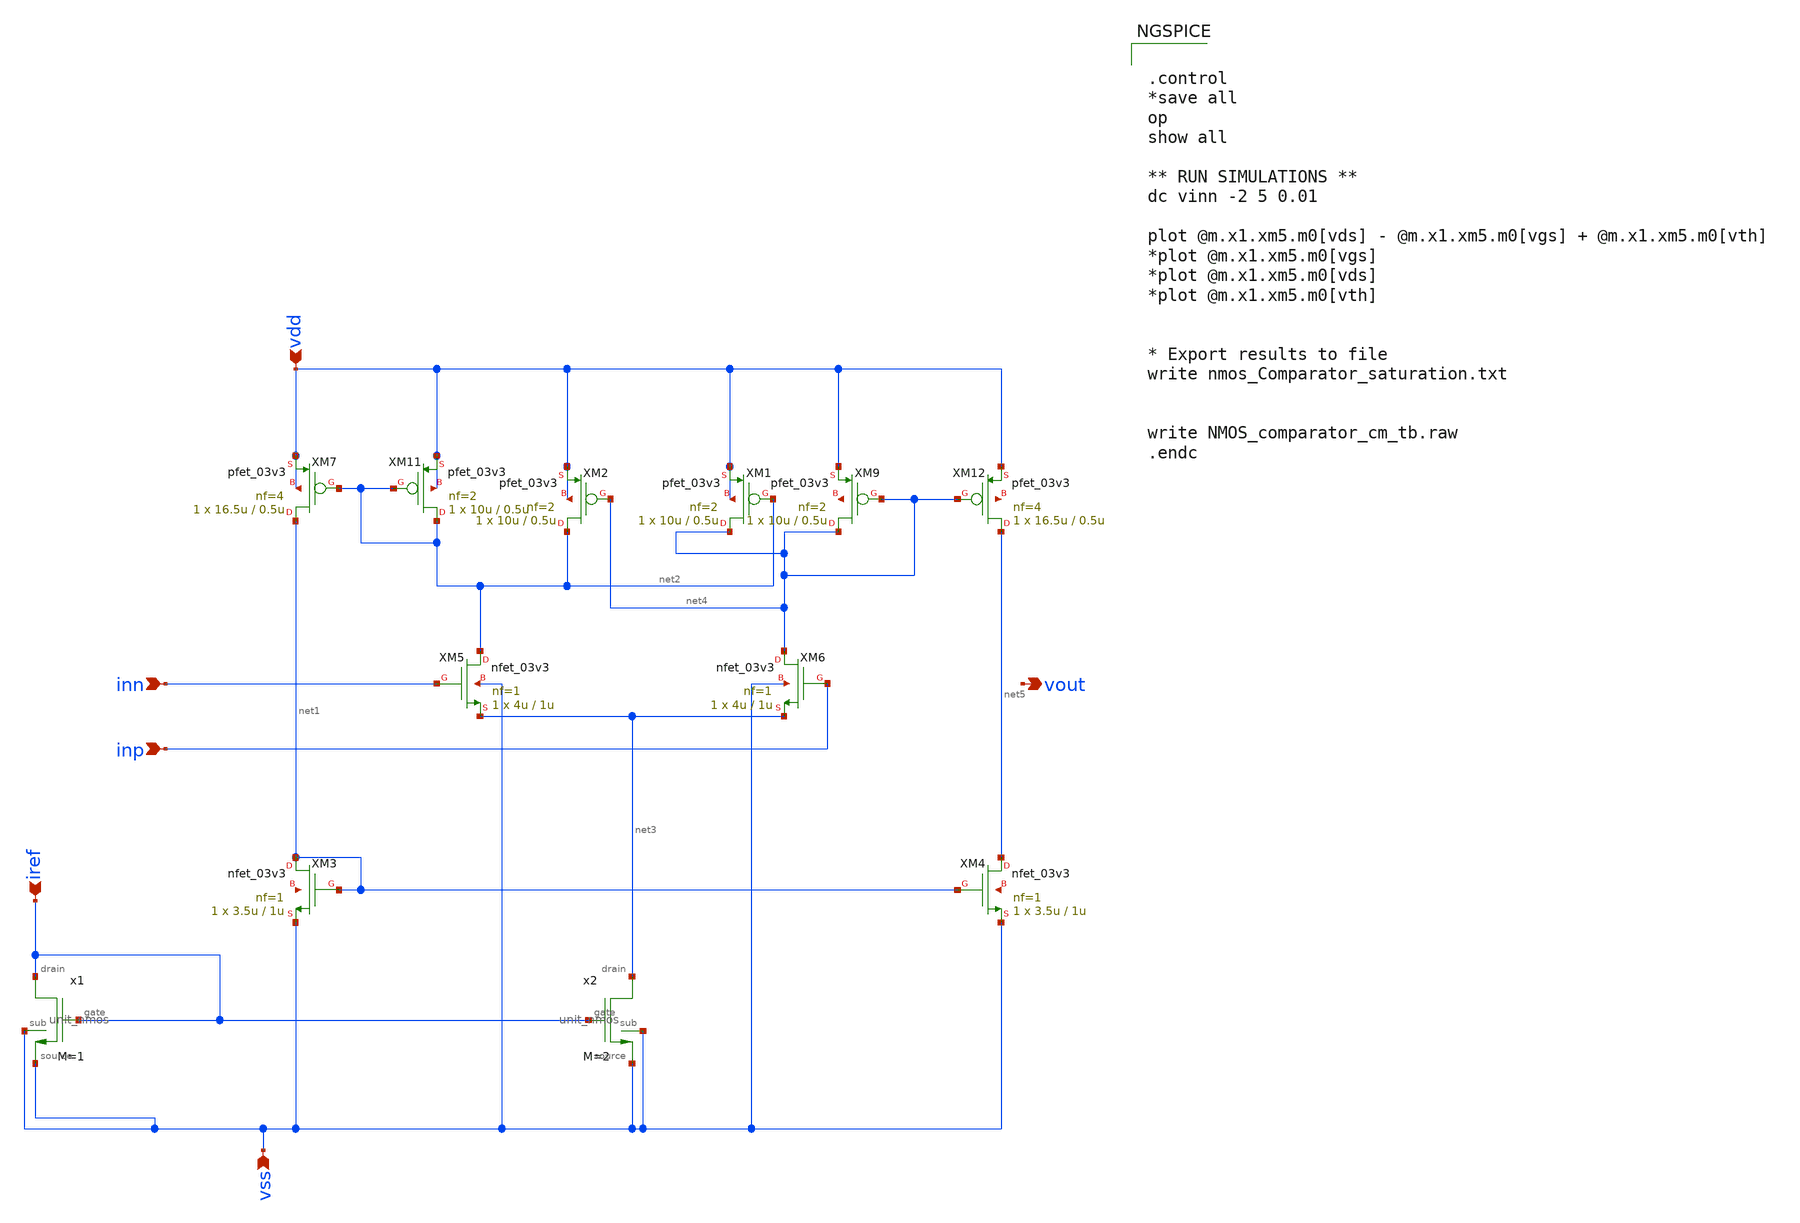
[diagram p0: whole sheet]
** sch_path: designs/libs/core_analog/Comparator/Nmos_Comparator.sch
**.subckt Nmos_Comparator vss vdd iref inn inp vout
*.ipin vss
*.ipin vdd
*.ipin iref
*.ipin inn
*.ipin inp
*.opin vout
XM3 net1 net1 vss net6 nfet_03v3 L=1u W=3.5u nf=1 ad='int((nf+1)/2) * W/nf * 0.18u' as='int((nf+2)/2) * W/nf * 0.18u'
+ pd='2*int((nf+1)/2) * (W/nf + 0.18u)' ps='2*int((nf+2)/2) * (W/nf + 0.18u)' nrd='0.18u / W' nrs='0.18u / W'
+ sa=0 sb=0 sd=0 m=1
XM4 net5 net1 vss net7 nfet_03v3 L=1u W=3.5u nf=1 ad='int((nf+1)/2) * W/nf * 0.18u' as='int((nf+2)/2) * W/nf * 0.18u'
+ pd='2*int((nf+1)/2) * (W/nf + 0.18u)' ps='2*int((nf+2)/2) * (W/nf + 0.18u)' nrd='0.18u / W' nrs='0.18u / W'
+ sa=0 sb=0 sd=0 m=1
XM5 net2 inn net3 vss nfet_03v3 L=1u W=4u nf=1 ad='int((nf+1)/2) * W/nf * 0.18u' as='int((nf+2)/2) * W/nf * 0.18u'
+ pd='2*int((nf+1)/2) * (W/nf + 0.18u)' ps='2*int((nf+2)/2) * (W/nf + 0.18u)' nrd='0.18u / W' nrs='0.18u / W'
+ sa=0 sb=0 sd=0 m=1
XM6 net4 inp net3 vss nfet_03v3 L=1u W=4u nf=1 ad='int((nf+1)/2) * W/nf * 0.18u' as='int((nf+2)/2) * W/nf * 0.18u'
+ pd='2*int((nf+1)/2) * (W/nf + 0.18u)' ps='2*int((nf+2)/2) * (W/nf + 0.18u)' nrd='0.18u / W' nrs='0.18u / W'
+ sa=0 sb=0 sd=0 m=1
XM7 net1 net2 vdd vdd pfet_03v3 L=0.5u W=16.5u nf=4 ad='int((nf+1)/2) * W/nf * 0.18u' as='int((nf+2)/2) * W/nf * 0.18u'
+ pd='2*int((nf+1)/2) * (W/nf + 0.18u)' ps='2*int((nf+2)/2) * (W/nf + 0.18u)' nrd='0.18u / W' nrs='0.18u / W'
+ sa=0 sb=0 sd=0 m=1
XM9 net4 net4 vdd net8 pfet_03v3 L=0.5u W=10u nf=2 ad='int((nf+1)/2) * W/nf * 0.18u' as='int((nf+2)/2) * W/nf * 0.18u'
+ pd='2*int((nf+1)/2) * (W/nf + 0.18u)' ps='2*int((nf+2)/2) * (W/nf + 0.18u)' nrd='0.18u / W' nrs='0.18u / W'
+ sa=0 sb=0 sd=0 m=1
XM11 net2 net2 vdd vdd pfet_03v3 L=0.5u W=10u nf=2 ad='int((nf+1)/2) * W/nf * 0.18u' as='int((nf+2)/2) * W/nf * 0.18u'
+ pd='2*int((nf+1)/2) * (W/nf + 0.18u)' ps='2*int((nf+2)/2) * (W/nf + 0.18u)' nrd='0.18u / W' nrs='0.18u / W'
+ sa=0 sb=0 sd=0 m=1
XM12 net5 net4 vdd net9 pfet_03v3 L=0.5u W=16.5u nf=4 ad='int((nf+1)/2) * W/nf * 0.18u' as='int((nf+2)/2) * W/nf * 0.18u'
+ pd='2*int((nf+1)/2) * (W/nf + 0.18u)' ps='2*int((nf+2)/2) * (W/nf + 0.18u)' nrd='0.18u / W' nrs='0.18u / W'
+ sa=0 sb=0 sd=0 m=1
x1 iref vss iref vss unit_nmos M=1
x2 net3 vss iref vss unit_nmos M=2
XM1 net4 net2 vdd vdd pfet_03v3 L=0.5u W=10u nf=2 ad='int((nf+1)/2) * W/nf * 0.18u' as='int((nf+2)/2) * W/nf * 0.18u'
+ pd='2*int((nf+1)/2) * (W/nf + 0.18u)' ps='2*int((nf+2)/2) * (W/nf + 0.18u)' nrd='0.18u / W' nrs='0.18u / W'
+ sa=0 sb=0 sd=0 m=1
XM2 net2 net4 vdd vdd pfet_03v3 L=0.5u W=10u nf=2 ad='int((nf+1)/2) * W/nf * 0.18u' as='int((nf+2)/2) * W/nf * 0.18u'
+ pd='2*int((nf+1)/2) * (W/nf + 0.18u)' ps='2*int((nf+2)/2) * (W/nf + 0.18u)' nrd='0.18u / W' nrs='0.18u / W'
+ sa=0 sb=0 sd=0 m=1
**** begin user architecture code


.control
*save all
op
show all

** RUN SIMULATIONS **
dc vinn -2 5 0.01

plot @m.x1.xm5.m0[vds] - @m.x1.xm5.m0[vgs] + @m.x1.xm5.m0[vth]
*plot @m.x1.xm5.m0[vgs]
*plot @m.x1.xm5.m0[vds]
*plot @m.x1.xm5.m0[vth]


* Export results to file
write nmos_Comparator_saturation.txt


write NMOS_comparator_cm_tb.raw
.endc


**** end user architecture code
**.ends

* expanding   symbol:  libs/core_analog/unit_nmos/unit_nmos.sym # of pins=4
** sym_path: libs/core_analog/unit_nmos/unit_nmos.sym
** sch_path: libs/core_analog/unit_nmos/unit_nmos.sch
.subckt unit_nmos drain sub gate source
*.iopin drain
*.iopin source
*.iopin sub
*.iopin gate
XM1 drain gate source sub nfet_03v3 L=1u W=2.5u nf=1 ad='int((nf+1)/2) * W/nf * 0.18u' as='int((nf+2)/2) * W/nf * 0.18u'
+ pd='2*int((nf+1)/2) * (W/nf + 0.18u)' ps='2*int((nf+2)/2) * (W/nf + 0.18u)' nrd='0.18u / W' nrs='0.18u / W'
+ sa=0 sb=0 sd=0 m={M}
**** begin user architecture code

.param M=1

**** end user architecture code
.ends

.end
